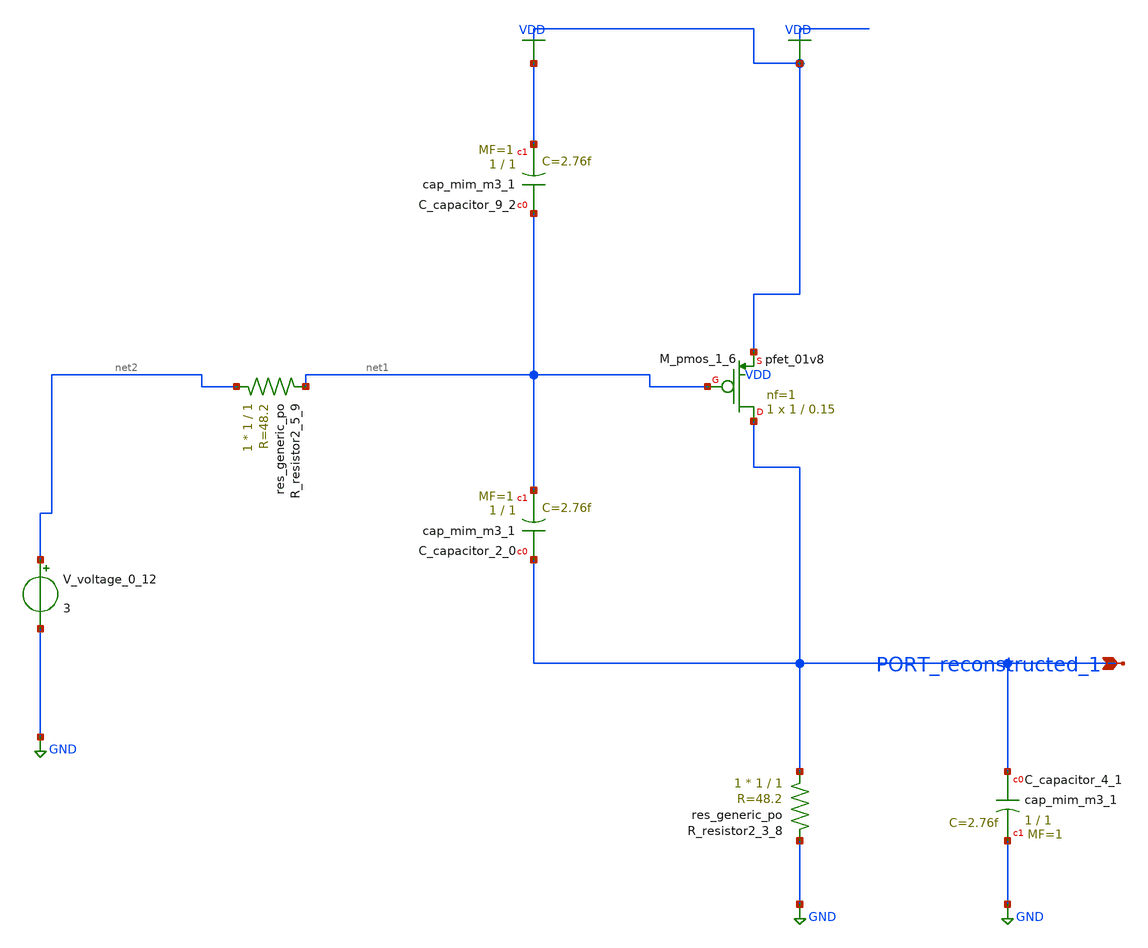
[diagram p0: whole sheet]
** sch_path: schematics/AMSNet/722.sch
**.subckt 722 PORT_reconstructed_1
*.ipin PORT_reconstructed_1
XC_capacitor_2_0 PORT_reconstructed_1 net1 sky130_fd_pr__cap_mim_m3_1 W=1 L=1 MF=1 m=1
XC_capacitor_4_1 PORT_reconstructed_1 GND sky130_fd_pr__cap_mim_m3_1 W=1 L=1 MF=1 m=1
XC_capacitor_9_2 net1 VDD sky130_fd_pr__cap_mim_m3_1 W=1 L=1 MF=1 m=1
XM_pmos_1_6 PORT_reconstructed_1 net1 VDD VDD sky130_fd_pr__pfet_01v8 L=0.15 W=1 nf=1 ad='int((1 + 1)/2) * 1 / 1 * 0.29'
+ as='int((1 + 2)/2) * 1 / 1 * 0.29' pd='2*int((1 + 1)/2) * (1 / 1 + 0.29)' ps='2*int((1 + 2)/2) * (1 / 1 + 0.29)'
+ nrd='0.29 / 1 ' nrs='0.29 / 1 ' sa=0 sb=0 sd=0 mult=1 m=1
XR_resistor2_3_8 PORT_reconstructed_1 GND sky130_fd_pr__res_generic_po W=1 L=1 m=1
XR_resistor2_5_9 net2 net1 sky130_fd_pr__res_generic_po W=1 L=1 m=1
V_voltage_0_12 net2 GND 3
**.ends
.GLOBAL GND
.GLOBAL VDD
.end
